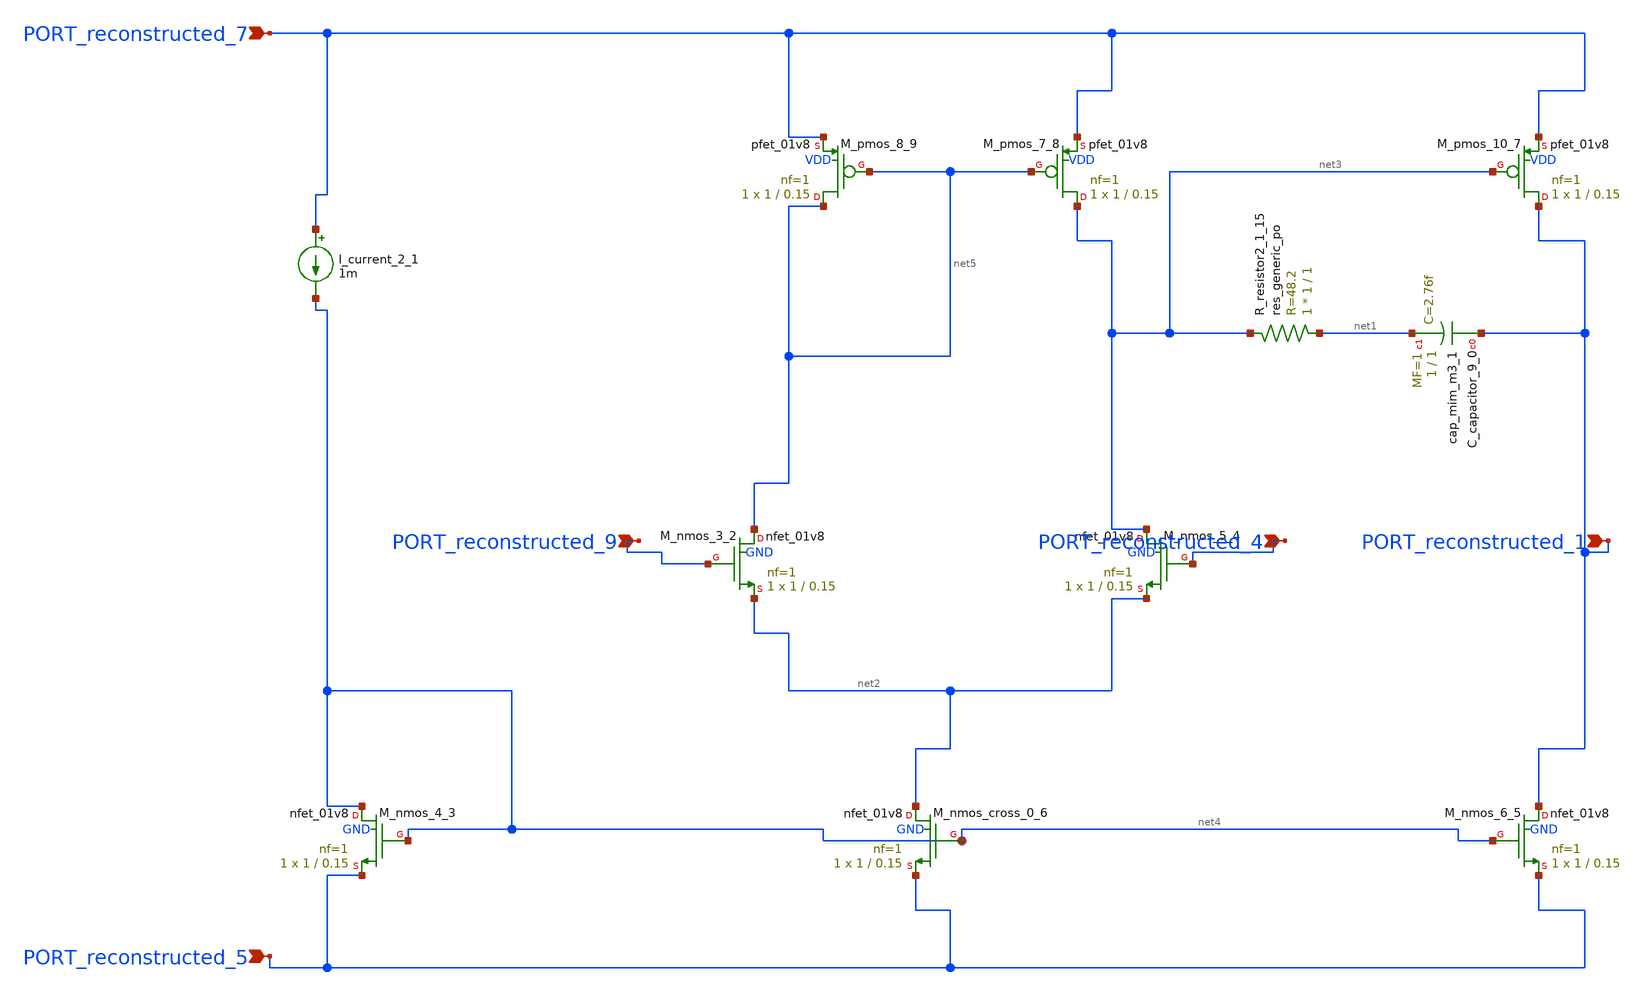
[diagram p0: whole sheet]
** sch_path: schematics/SchemGen/p06_fig1_target_op_amp.sch
**.subckt p06_fig1_target_op_amp PORT_reconstructed_1 PORT_reconstructed_9 PORT_reconstructed_4
*+ PORT_reconstructed_5 PORT_reconstructed_7
*.ipin PORT_reconstructed_1
*.ipin PORT_reconstructed_9
*.ipin PORT_reconstructed_4
*.ipin PORT_reconstructed_5
*.ipin PORT_reconstructed_7
XC_capacitor_9_0 PORT_reconstructed_1 net1 sky130_fd_pr__cap_mim_m3_1 W=1 L=1 MF=1 m=1
I_current_2_1 PORT_reconstructed_7 net4 1m
XM_nmos_3_2 net5 PORT_reconstructed_9 net2 GND sky130_fd_pr__nfet_01v8 L=0.15 W=1 nf=1 ad='int((1 + 1)/2) * 1 / 1 * 0.29'
+ as='int((1 + 2)/2) * 1 / 1 * 0.29' pd='2*int((1 + 1)/2) * (1 / 1 + 0.29)' ps='2*int((1 + 2)/2) * (1 / 1 + 0.29)'
+ nrd='0.29 / 1 ' nrs='0.29 / 1 ' sa=0 sb=0 sd=0 mult=1 m=1
XM_nmos_4_3 net4 net4 PORT_reconstructed_5 GND sky130_fd_pr__nfet_01v8 L=0.15 W=1 nf=1 ad='int((1 + 1)/2) * 1 / 1 * 0.29'
+ as='int((1 + 2)/2) * 1 / 1 * 0.29' pd='2*int((1 + 1)/2) * (1 / 1 + 0.29)' ps='2*int((1 + 2)/2) * (1 / 1 + 0.29)'
+ nrd='0.29 / 1 ' nrs='0.29 / 1 ' sa=0 sb=0 sd=0 mult=1 m=1
XM_nmos_5_4 net3 PORT_reconstructed_4 net2 GND sky130_fd_pr__nfet_01v8 L=0.15 W=1 nf=1 ad='int((1 + 1)/2) * 1 / 1 * 0.29'
+ as='int((1 + 2)/2) * 1 / 1 * 0.29' pd='2*int((1 + 1)/2) * (1 / 1 + 0.29)' ps='2*int((1 + 2)/2) * (1 / 1 + 0.29)'
+ nrd='0.29 / 1 ' nrs='0.29 / 1 ' sa=0 sb=0 sd=0 mult=1 m=1
XM_nmos_6_5 PORT_reconstructed_1 net4 PORT_reconstructed_5 GND sky130_fd_pr__nfet_01v8 L=0.15 W=1 nf=1
+ ad='int((1 + 1)/2) * 1 / 1 * 0.29' as='int((1 + 2)/2) * 1 / 1 * 0.29' pd='2*int((1 + 1)/2) * (1 / 1 + 0.29)'
+ ps='2*int((1 + 2)/2) * (1 / 1 + 0.29)' nrd='0.29 / 1 ' nrs='0.29 / 1 ' sa=0 sb=0 sd=0 mult=1 m=1
XM_nmos_cross_0_6 net2 net4 PORT_reconstructed_5 GND sky130_fd_pr__nfet_01v8 L=0.15 W=1 nf=1 ad='int((1 + 1)/2) * 1 / 1 * 0.29'
+ as='int((1 + 2)/2) * 1 / 1 * 0.29' pd='2*int((1 + 1)/2) * (1 / 1 + 0.29)' ps='2*int((1 + 2)/2) * (1 / 1 + 0.29)'
+ nrd='0.29 / 1 ' nrs='0.29 / 1 ' sa=0 sb=0 sd=0 mult=1 m=1
XM_pmos_10_7 PORT_reconstructed_1 net3 PORT_reconstructed_7 VDD sky130_fd_pr__pfet_01v8 L=0.15 W=1 nf=1
+ ad='int((1 + 1)/2) * 1 / 1 * 0.29' as='int((1 + 2)/2) * 1 / 1 * 0.29' pd='2*int((1 + 1)/2) * (1 / 1 + 0.29)'
+ ps='2*int((1 + 2)/2) * (1 / 1 + 0.29)' nrd='0.29 / 1 ' nrs='0.29 / 1 ' sa=0 sb=0 sd=0 mult=1 m=1
XM_pmos_7_8 net3 net5 PORT_reconstructed_7 VDD sky130_fd_pr__pfet_01v8 L=0.15 W=1 nf=1 ad='int((1 + 1)/2) * 1 / 1 * 0.29'
+ as='int((1 + 2)/2) * 1 / 1 * 0.29' pd='2*int((1 + 1)/2) * (1 / 1 + 0.29)' ps='2*int((1 + 2)/2) * (1 / 1 + 0.29)'
+ nrd='0.29 / 1 ' nrs='0.29 / 1 ' sa=0 sb=0 sd=0 mult=1 m=1
XM_pmos_8_9 net5 net5 PORT_reconstructed_7 VDD sky130_fd_pr__pfet_01v8 L=0.15 W=1 nf=1 ad='int((1 + 1)/2) * 1 / 1 * 0.29'
+ as='int((1 + 2)/2) * 1 / 1 * 0.29' pd='2*int((1 + 1)/2) * (1 / 1 + 0.29)' ps='2*int((1 + 2)/2) * (1 / 1 + 0.29)'
+ nrd='0.29 / 1 ' nrs='0.29 / 1 ' sa=0 sb=0 sd=0 mult=1 m=1
XR_resistor2_1_15 net1 net3 sky130_fd_pr__res_generic_po W=1 L=1 m=1
**.ends
.end
